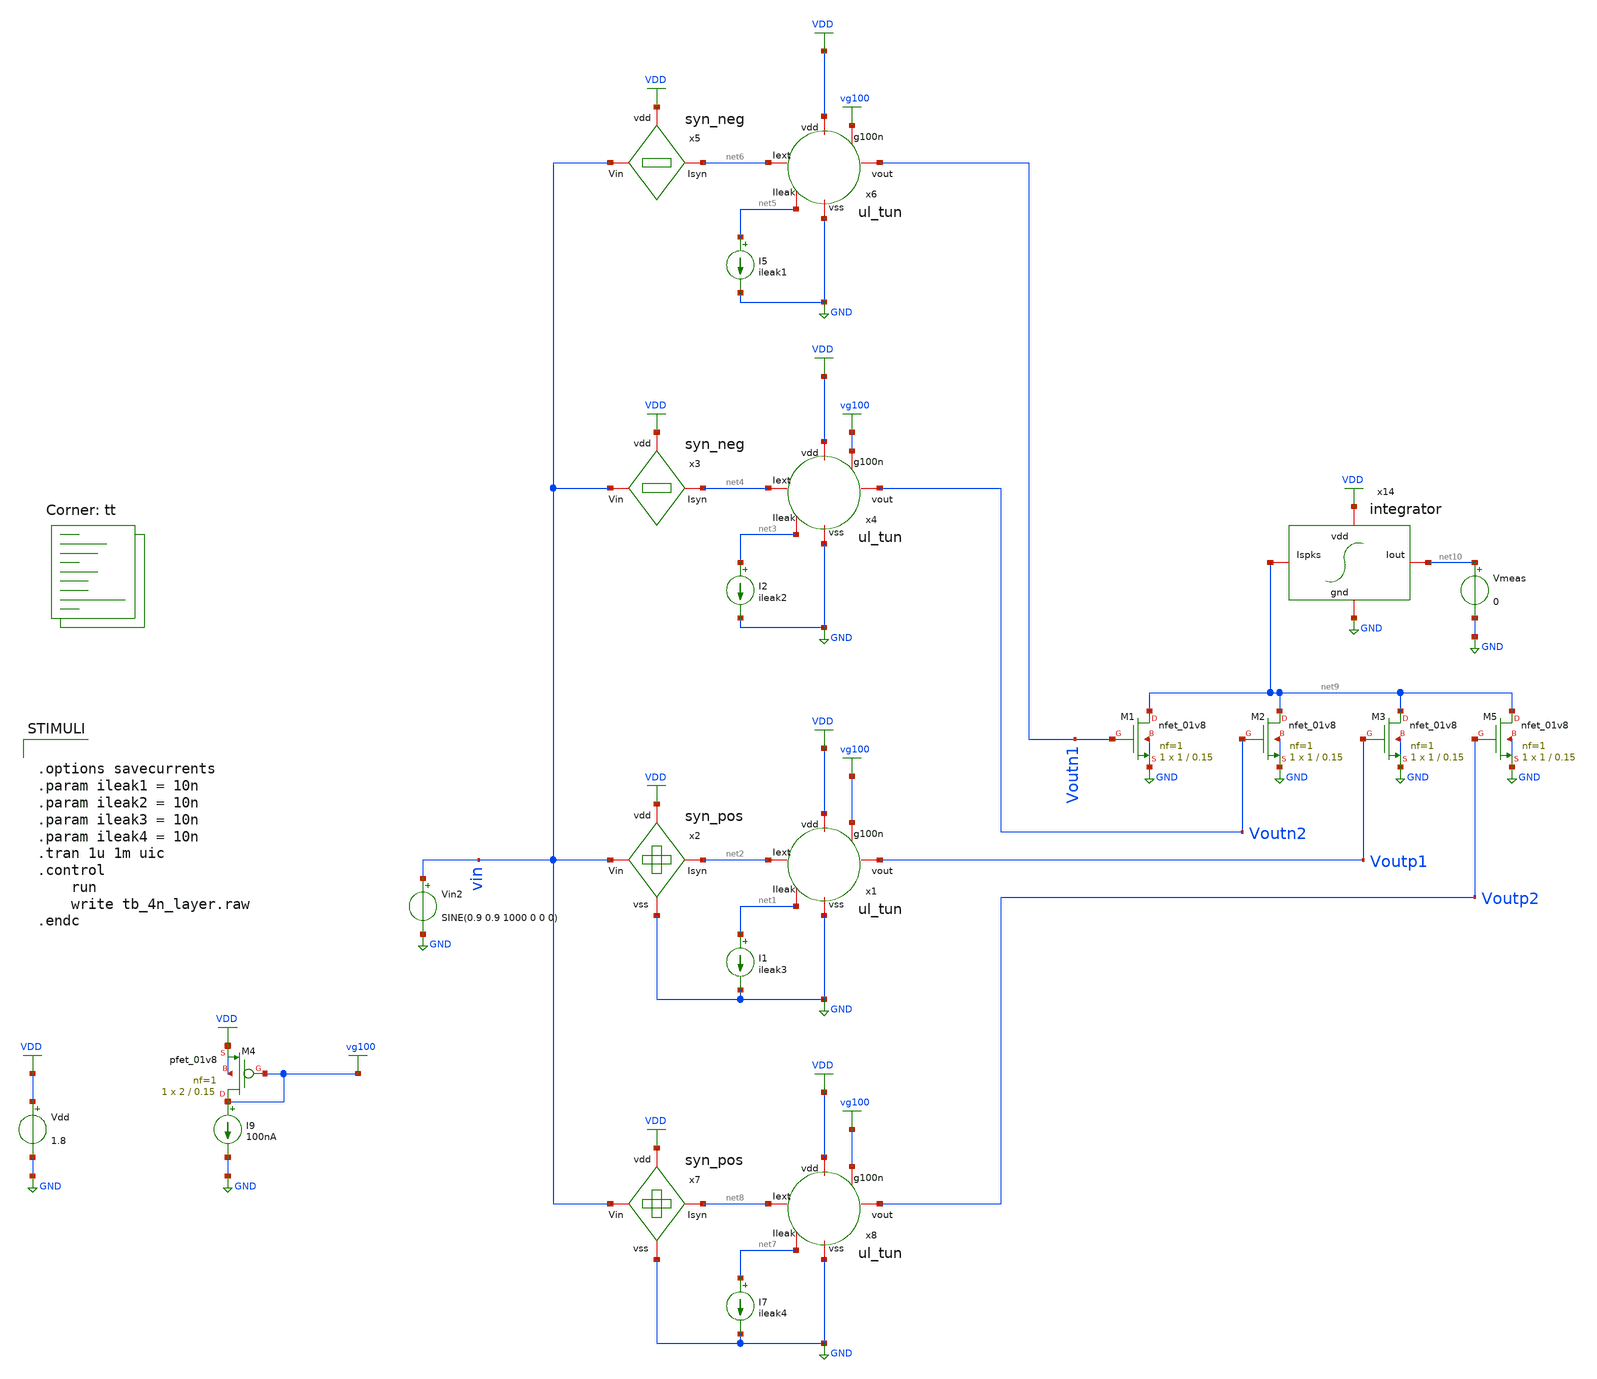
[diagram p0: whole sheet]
** sch_path: Neuron/ultralif/tb_4n_layer.sch
**.subckt tb_4n_layer
I1 net1 GND ileak3
Vdd VDD GND 1.8
x2 VDD vin net2 GND syn_pos
x1 net2 VDD vg100 Voutp1 net1 GND ul_tun
I2 net3 GND ileak2
x3 VDD vin net4 syn_neg
x4 net4 VDD vg100 Voutn2 net3 GND ul_tun
I5 net5 GND ileak1
x5 VDD vin net6 syn_neg
x6 net6 VDD vg100 Voutn1 net5 GND ul_tun
I7 net7 GND ileak4
x7 VDD vin net8 GND syn_pos
x8 net8 VDD vg100 Voutp2 net7 GND ul_tun
I9 vg100 GND 100nA
XM4 vg100 vg100 VDD VDD sky130_fd_pr__pfet_01v8 L=0.15 W=2 nf=1 ad='int((nf+1)/2) * W/nf * 0.29' as='int((nf+2)/2) * W/nf * 0.29'
+ pd='2*int((nf+1)/2) * (W/nf + 0.29)' ps='2*int((nf+2)/2) * (W/nf + 0.29)' nrd='0.29 / W' nrs='0.29 / W'
+ sa=0 sb=0 sd=0 mult=1 m=1
x14 VDD net10 net9 GND integrator
XM1 net9 Voutn1 GND GND sky130_fd_pr__nfet_01v8 L=0.15 W=1 nf=1 ad='int((nf+1)/2) * W/nf * 0.29' as='int((nf+2)/2) * W/nf * 0.29'
+ pd='2*int((nf+1)/2) * (W/nf + 0.29)' ps='2*int((nf+2)/2) * (W/nf + 0.29)' nrd='0.29 / W' nrs='0.29 / W'
+ sa=0 sb=0 sd=0 mult=1 m=1
XM2 net9 Voutn2 GND GND sky130_fd_pr__nfet_01v8 L=0.15 W=1 nf=1 ad='int((nf+1)/2) * W/nf * 0.29' as='int((nf+2)/2) * W/nf * 0.29'
+ pd='2*int((nf+1)/2) * (W/nf + 0.29)' ps='2*int((nf+2)/2) * (W/nf + 0.29)' nrd='0.29 / W' nrs='0.29 / W'
+ sa=0 sb=0 sd=0 mult=1 m=1
XM3 net9 Voutp1 GND GND sky130_fd_pr__nfet_01v8 L=0.15 W=1 nf=1 ad='int((nf+1)/2) * W/nf * 0.29' as='int((nf+2)/2) * W/nf * 0.29'
+ pd='2*int((nf+1)/2) * (W/nf + 0.29)' ps='2*int((nf+2)/2) * (W/nf + 0.29)' nrd='0.29 / W' nrs='0.29 / W'
+ sa=0 sb=0 sd=0 mult=1 m=1
XM5 net9 Voutp2 GND GND sky130_fd_pr__nfet_01v8 L=0.15 W=1 nf=1 ad='int((nf+1)/2) * W/nf * 0.29' as='int((nf+2)/2) * W/nf * 0.29'
+ pd='2*int((nf+1)/2) * (W/nf + 0.29)' ps='2*int((nf+2)/2) * (W/nf + 0.29)' nrd='0.29 / W' nrs='0.29 / W'
+ sa=0 sb=0 sd=0 mult=1 m=1
Vmeas net10 GND 0
Vin2 vin GND SINE(0.9 0.9 1000 0 0 0)
**** begin user architecture code
.lib $::SKYWATER_MODELS/sky130.lib.spice tt
**** end user architecture code
**.ends

* expanding   symbol:  syn_pos.sym # of pins=4
** sym_path: Neuron/ultralif/syn_pos.sym
** sch_path: Neuron/ultralif/syn_pos.sch
.subckt syn_pos vdd Vin Isyn vss
*.iopin Vin
*.iopin vdd
*.iopin vss
*.iopin Isyn
XM9 Isyn vx vdd vdd sky130_fd_pr__pfet_01v8 L=1 W=0.5 nf=1 ad='int((nf+1)/2) * W/nf * 0.29' as='int((nf+2)/2) * W/nf * 0.29'
+ pd='2*int((nf+1)/2) * (W/nf + 0.29)' ps='2*int((nf+2)/2) * (W/nf + 0.29)' nrd='0.29 / W' nrs='0.29 / W'
+ sa=0 sb=0 sd=0 mult=1 m=1
XM10 vx vx vdd vdd sky130_fd_pr__pfet_01v8 L=0.15 W=0.5 nf=1 ad='int((nf+1)/2) * W/nf * 0.29' as='int((nf+2)/2) * W/nf * 0.29'
+ pd='2*int((nf+1)/2) * (W/nf + 0.29)' ps='2*int((nf+2)/2) * (W/nf + 0.29)' nrd='0.29 / W' nrs='0.29 / W'
+ sa=0 sb=0 sd=0 mult=5 m=5
XM12 vx Vin vss vss sky130_fd_pr__nfet_01v8 L=1 W=0.4 nf=1 ad='int((1 + 1)/2) * 0.4 / 1 * 0.29' as='int((1 + 2)/2) * 0.4 / 1 * 0.29'
+ pd='2*int((1 + 1)/2) * (0.4 / 1 + 0.29)' ps='2*int((1 + 2)/2) * (0.4 / 1 + 0.29)' nrd='0.29 / 0.4 ' nrs='0.29 / 0.4 '
+ sa=0 sb=0 sd=0 mult=1 m=1
.ends


* expanding   symbol:  ul_tun.sym # of pins=6
** sym_path: Neuron/ultralif/ul_tun.sym
** sch_path: Neuron/ultralif/ul_tun.sch
.subckt ul_tun Iext vdd g100n vout Ileak vss
*.iopin Iext
*.iopin vout
*.iopin vss
*.iopin Ileak
*.iopin vdd
*.iopin g100n
XM1 Ileak Ileak net1 vdd sky130_fd_pr__pfet_01v8 L=10 W=1 nf=1 ad='int((nf+1)/2) * W/nf * 0.29' as='int((nf+2)/2) * W/nf * 0.29'
+ pd='2*int((nf+1)/2) * (W/nf + 0.29)' ps='2*int((nf+2)/2) * (W/nf + 0.29)' nrd='0.29 / W' nrs='0.29 / W'
+ sa=0 sb=0 sd=0 mult=1 m=1
XM2 Ileak net2 net1 vdd sky130_fd_pr__pfet_01v8 L=0.15 W=1.5 nf=1 ad='int((nf+1)/2) * W/nf * 0.29' as='int((nf+2)/2) * W/nf * 0.29'
+ pd='2*int((nf+1)/2) * (W/nf + 0.29)' ps='2*int((nf+2)/2) * (W/nf + 0.29)' nrd='0.29 / W' nrs='0.29 / W'
+ sa=0 sb=0 sd=0 mult=1 m=1
XM3 net2 net2 net1 vdd sky130_fd_pr__pfet_01v8 L=0.15 W=15 nf=1 ad='int((nf+1)/2) * W/nf * 0.29' as='int((nf+2)/2) * W/nf * 0.29'
+ pd='2*int((nf+1)/2) * (W/nf + 0.29)' ps='2*int((nf+2)/2) * (W/nf + 0.29)' nrd='0.29 / W' nrs='0.29 / W'
+ sa=0 sb=0 sd=0 mult=1 m=1
XM4 net2 Ileak vss vss sky130_fd_pr__nfet_01v8 L=4 W=1 nf=1 ad='int((1 + 1)/2) * 1 / 1 * 0.29' as='int((1 + 2)/2) * 1 / 1 * 0.29'
+ pd='2*int((1 + 1)/2) * (1 / 1 + 0.29)' ps='2*int((1 + 2)/2) * (1 / 1 + 0.29)' nrd='0.29 / 1 ' nrs='0.29 / 1 '
+ sa=0 sb=0 sd=0 mult=1 m=1
C1 net1 vss 1p m=1
XM5 vout_n Ileak vss vss sky130_fd_pr__nfet_01v8 L=0.15 W=1 nf=1 ad='int((1 + 1)/2) * 1 / 1 * 0.29' as='int((1 + 2)/2) * 1 / 1 * 0.29'
+ pd='2*int((1 + 1)/2) * (1 / 1 + 0.29)' ps='2*int((1 + 2)/2) * (1 / 1 + 0.29)' nrd='0.29 / 1 ' nrs='0.29 / 1 '
+ sa=0 sb=0 sd=0 mult=1 m=1
XM6 vout_n g100n vdd vdd sky130_fd_pr__pfet_01v8 L=0.15 W=2 nf=1 ad='int((nf+1)/2) * W/nf * 0.29' as='int((nf+2)/2) * W/nf * 0.29'
+ pd='2*int((nf+1)/2) * (W/nf + 0.29)' ps='2*int((nf+2)/2) * (W/nf + 0.29)' nrd='0.29 / W' nrs='0.29 / W'
+ sa=0 sb=0 sd=0 mult=1 m=1
XM7 vout vout_n vss vss sky130_fd_pr__nfet_01v8 L=0.15 W=1 nf=1 ad='int((1 + 1)/2) * 1 / 1 * 0.29' as='int((1 + 2)/2) * 1 / 1 * 0.29'
+ pd='2*int((1 + 1)/2) * (1 / 1 + 0.29)' ps='2*int((1 + 2)/2) * (1 / 1 + 0.29)' nrd='0.29 / 1 ' nrs='0.29 / 1 '
+ sa=0 sb=0 sd=0 mult=1 m=1
XM8 vout vout_n vdd vdd sky130_fd_pr__pfet_01v8 L=0.15 W=2 nf=1 ad='int((nf+1)/2) * W/nf * 0.29' as='int((nf+2)/2) * W/nf * 0.29'
+ pd='2*int((nf+1)/2) * (W/nf + 0.29)' ps='2*int((nf+2)/2) * (W/nf + 0.29)' nrd='0.29 / W' nrs='0.29 / W'
+ sa=0 sb=0 sd=0 mult=1 m=1
vext Iext net1 0
**** begin user architecture code


.save i(vext)


**** end user architecture code
.ends


* expanding   symbol:  syn_neg.sym # of pins=3
** sym_path: Neuron/ultralif/syn_neg.sym
** sch_path: Neuron/ultralif/syn_neg.sch
.subckt syn_neg vdd Vin Isyn
*.iopin Vin
*.iopin Isyn
*.iopin vdd
XM10 Isyn Vin vx vdd sky130_fd_pr__pfet_01v8 L=30 W=0.5 nf=1 ad='int((nf+1)/2) * W/nf * 0.29' as='int((nf+2)/2) * W/nf * 0.29'
+ pd='2*int((nf+1)/2) * (W/nf + 0.29)' ps='2*int((nf+2)/2) * (W/nf + 0.29)' nrd='0.29 / W' nrs='0.29 / W'
+ sa=0 sb=0 sd=0 mult=1 m=1
XM1 vx Vin vdd vdd sky130_fd_pr__pfet_01v8 L=30 W=0.5 nf=1 ad='int((nf+1)/2) * W/nf * 0.29' as='int((nf+2)/2) * W/nf * 0.29'
+ pd='2*int((nf+1)/2) * (W/nf + 0.29)' ps='2*int((nf+2)/2) * (W/nf + 0.29)' nrd='0.29 / W' nrs='0.29 / W'
+ sa=0 sb=0 sd=0 mult=1 m=1
.ends


* expanding   symbol:  integrator.sym # of pins=4
** sym_path: Neuron/ultralif/integrator.sym
** sch_path: Neuron/ultralif/integrator.sch
.subckt integrator vdd Iout Ispks gnd
*.iopin Ispks
*.iopin Iout
*.iopin vdd
*.iopin gnd
XMIn Ispks vx vsyn vdd sky130_fd_pr__pfet_01v8 L=0.15 W=5 nf=1 ad='int((nf+1)/2) * W/nf * 0.29' as='int((nf+2)/2) * W/nf * 0.29'
+ pd='2*int((nf+1)/2) * (W/nf + 0.29)' ps='2*int((nf+2)/2) * (W/nf + 0.29)' nrd='0.29 / W' nrs='0.29 / W'
+ sa=0 sb=0 sd=0 mult=1 m=1
XM3 vsyn vdd vdd vdd sky130_fd_pr__pfet_01v8 L=0.15 W=5 nf=1 ad='int((nf+1)/2) * W/nf * 0.29' as='int((nf+2)/2) * W/nf * 0.29'
+ pd='2*int((nf+1)/2) * (W/nf + 0.29)' ps='2*int((nf+2)/2) * (W/nf + 0.29)' nrd='0.29 / W' nrs='0.29 / W'
+ sa=0 sb=0 sd=0 mult=1 m=1
XM4 Iout vsyn vdd vdd sky130_fd_pr__pfet_01v8 L=0.15 W=24.5 nf=1 ad='int((nf+1)/2) * W/nf * 0.29' as='int((nf+2)/2) * W/nf * 0.29'
+ pd='2*int((nf+1)/2) * (W/nf + 0.29)' ps='2*int((nf+2)/2) * (W/nf + 0.29)' nrd='0.29 / W' nrs='0.29 / W'
+ sa=0 sb=0 sd=0 mult=1 m=1
XCsyn vdd vsyn sky130_fd_pr__cap_mim_m3_1 W=22.5 L=22 MF=1 m=1
XR2 vx vdd sky130_fd_pr__res_generic_po W=1 L=1 m=1
XR1 gnd vx sky130_fd_pr__res_generic_po W=1 L=1 m=1
.ends

.GLOBAL GND
.GLOBAL VDD
.GLOBAL vg100
**** begin user architecture code


.options savecurrents
.param ileak1 = 10n
.param ileak2 = 10n
.param ileak3 = 10n
.param ileak4 = 10n
.tran 1u 1m uic
.control
	run
	write tb_4n_layer.raw
.endc


**** end user architecture code
.end
